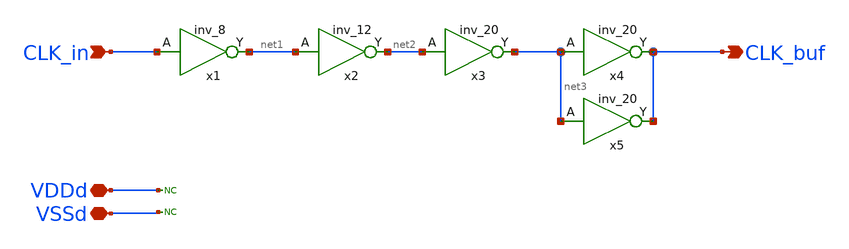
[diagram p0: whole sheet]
** sch_path: PHI_CLK_buf/PHI_CLK_buf.sch
**.subckt PHI_CLK_buf CLK_in CLK_buf VDDd VSSd
*.ipin CLK_in
*.opin CLK_buf
*.iopin VDDd
*.iopin VSSd
x1 CLK_in VSSd VDDd VSSd VDDd net1 gf180mcu_fd_sc_mcu9t5v0__inv_8
x2 net1 VSSd VDDd VSSd VDDd net2 gf180mcu_fd_sc_mcu9t5v0__inv_12
x4 net3 CLK_buf VDDd VDDd VSSd VSSd gf180mcu_fd_sc_mcu9t5v0__inv_20
x3 net2 net3 VDDd VDDd VSSd VSSd gf180mcu_fd_sc_mcu9t5v0__inv_20
x5 net3 CLK_buf VDDd VDDd VSSd VSSd gf180mcu_fd_sc_mcu9t5v0__inv_20
* noconn VDDd
* noconn VSSd
**.ends
.end
